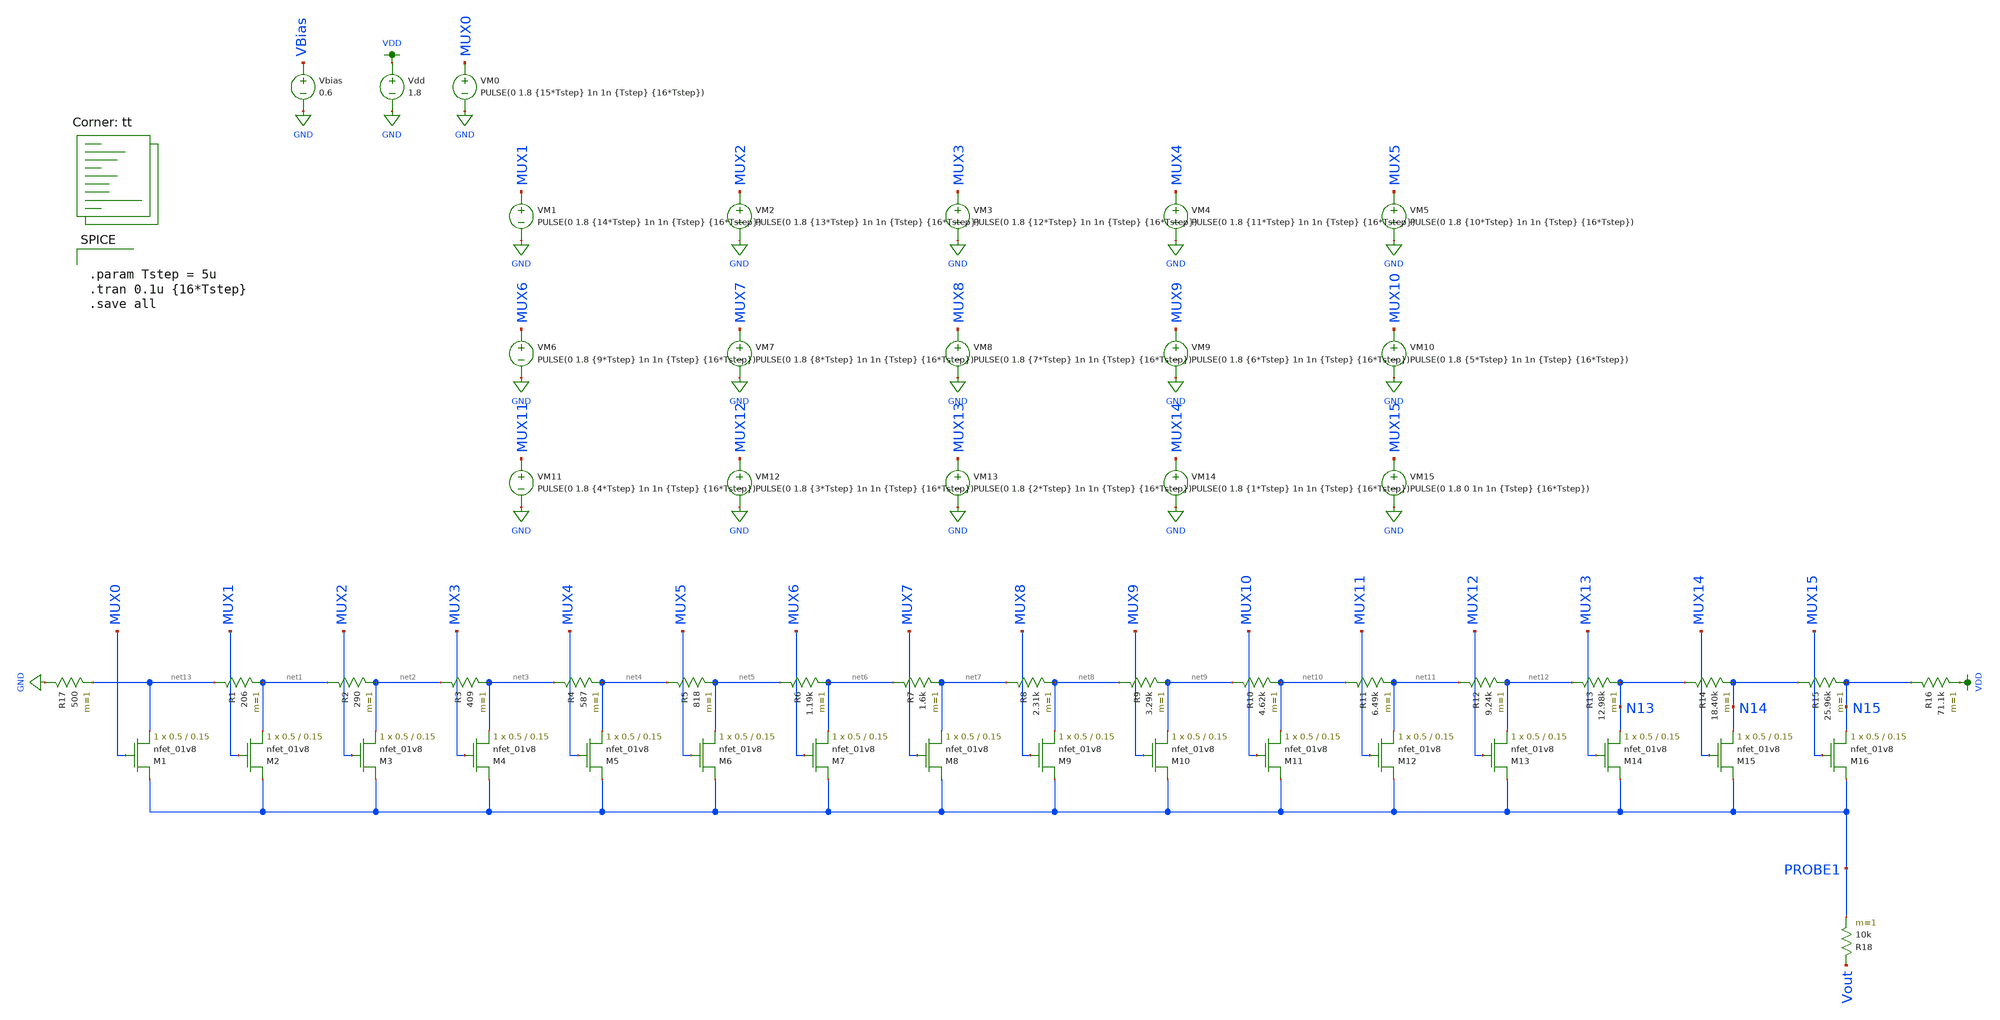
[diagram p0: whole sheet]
** sch_path: DAC/DAC2TB.sch
**.subckt DAC2TB
Vdd VDD GND 1.8
R1 net13 net1 206 m=1
R2 net1 net2 290 m=1
R3 net2 net3 409 m=1
R4 net3 net4 587 m=1
R5 net4 net5 818 m=1
R6 net5 net6 1.19k m=1
R7 net6 net7 1.6k m=1
R8 net7 net8 2.31k m=1
R9 net8 net9 3.29k m=1
R10 net9 net10 4.62k m=1
R11 net10 net11 6.49k m=1
R12 net11 net12 9.24k m=1
R13 net12 N13 12.98k m=1
R14 N13 N14 18.40k m=1
R15 N14 N15 25.96k m=1
R16 N15 VDD 71.1k m=1
XM1 PROBE1 MUX0 net13 GND sky130_fd_pr__nfet_01v8 L=0.15 W=0.5 nf=1 ad='int((nf+1)/2) * W/nf * 0.29'
+ as='int((nf+2)/2) * W/nf * 0.29' pd='2*int((nf+1)/2) * (W/nf + 0.29)' ps='2*int((nf+2)/2) * (W/nf + 0.29)'
+ nrd='0.29 / W' nrs='0.29 / W' sa=0 sb=0 sd=0 mult=1 m=1
VM1 MUX1 GND PULSE(0 1.8 {14*Tstep} 1n 1n {Tstep} {16*Tstep})
VM2 MUX2 GND PULSE(0 1.8 {13*Tstep} 1n 1n {Tstep} {16*Tstep})
VM3 MUX3 GND PULSE(0 1.8 {12*Tstep} 1n 1n {Tstep} {16*Tstep})
VM4 MUX4 GND PULSE(0 1.8 {11*Tstep} 1n 1n {Tstep} {16*Tstep})
VM5 MUX5 GND PULSE(0 1.8 {10*Tstep} 1n 1n {Tstep} {16*Tstep})
VM6 MUX6 GND PULSE(0 1.8 {9*Tstep} 1n 1n {Tstep} {16*Tstep})
VM7 MUX7 GND PULSE(0 1.8 {8*Tstep} 1n 1n {Tstep} {16*Tstep})
VM8 MUX8 GND PULSE(0 1.8 {7*Tstep} 1n 1n {Tstep} {16*Tstep})
VM9 MUX9 GND PULSE(0 1.8 {6*Tstep} 1n 1n {Tstep} {16*Tstep})
VM10 MUX10 GND PULSE(0 1.8 {5*Tstep} 1n 1n {Tstep} {16*Tstep})
VM11 MUX11 GND PULSE(0 1.8 {4*Tstep} 1n 1n {Tstep} {16*Tstep})
VM12 MUX12 GND PULSE(0 1.8 {3*Tstep} 1n 1n {Tstep} {16*Tstep})
VM13 MUX13 GND PULSE(0 1.8 {2*Tstep} 1n 1n {Tstep} {16*Tstep})
VM14 MUX14 GND PULSE(0 1.8 {1*Tstep} 1n 1n {Tstep} {16*Tstep})
VM15 MUX15 GND PULSE(0 1.8 0 1n 1n {Tstep} {16*Tstep})
VM0 MUX0 GND PULSE(0 1.8 {15*Tstep} 1n 1n {Tstep} {16*Tstep})
Vbias VBias GND 0.6
R17 GND net13 500 m=1
R18 Vout PROBE1 10k m=1
XM2 PROBE1 MUX1 net1 GND sky130_fd_pr__nfet_01v8 L=0.15 W=0.5 nf=1 ad='int((nf+1)/2) * W/nf * 0.29' as='int((nf+2)/2) * W/nf * 0.29'
+ pd='2*int((nf+1)/2) * (W/nf + 0.29)' ps='2*int((nf+2)/2) * (W/nf + 0.29)' nrd='0.29 / W' nrs='0.29 / W'
+ sa=0 sb=0 sd=0 mult=1 m=1
XM3 PROBE1 MUX2 net2 GND sky130_fd_pr__nfet_01v8 L=0.15 W=0.5 nf=1 ad='int((nf+1)/2) * W/nf * 0.29' as='int((nf+2)/2) * W/nf * 0.29'
+ pd='2*int((nf+1)/2) * (W/nf + 0.29)' ps='2*int((nf+2)/2) * (W/nf + 0.29)' nrd='0.29 / W' nrs='0.29 / W'
+ sa=0 sb=0 sd=0 mult=1 m=1
XM4 PROBE1 MUX3 net3 GND sky130_fd_pr__nfet_01v8 L=0.15 W=0.5 nf=1 ad='int((nf+1)/2) * W/nf * 0.29' as='int((nf+2)/2) * W/nf * 0.29'
+ pd='2*int((nf+1)/2) * (W/nf + 0.29)' ps='2*int((nf+2)/2) * (W/nf + 0.29)' nrd='0.29 / W' nrs='0.29 / W'
+ sa=0 sb=0 sd=0 mult=1 m=1
XM5 PROBE1 MUX4 net4 GND sky130_fd_pr__nfet_01v8 L=0.15 W=0.5 nf=1 ad='int((nf+1)/2) * W/nf * 0.29' as='int((nf+2)/2) * W/nf * 0.29'
+ pd='2*int((nf+1)/2) * (W/nf + 0.29)' ps='2*int((nf+2)/2) * (W/nf + 0.29)' nrd='0.29 / W' nrs='0.29 / W'
+ sa=0 sb=0 sd=0 mult=1 m=1
XM6 PROBE1 MUX5 net5 GND sky130_fd_pr__nfet_01v8 L=0.15 W=0.5 nf=1 ad='int((nf+1)/2) * W/nf * 0.29' as='int((nf+2)/2) * W/nf * 0.29'
+ pd='2*int((nf+1)/2) * (W/nf + 0.29)' ps='2*int((nf+2)/2) * (W/nf + 0.29)' nrd='0.29 / W' nrs='0.29 / W'
+ sa=0 sb=0 sd=0 mult=1 m=1
XM7 PROBE1 MUX6 net6 GND sky130_fd_pr__nfet_01v8 L=0.15 W=0.5 nf=1 ad='int((nf+1)/2) * W/nf * 0.29' as='int((nf+2)/2) * W/nf * 0.29'
+ pd='2*int((nf+1)/2) * (W/nf + 0.29)' ps='2*int((nf+2)/2) * (W/nf + 0.29)' nrd='0.29 / W' nrs='0.29 / W'
+ sa=0 sb=0 sd=0 mult=1 m=1
XM8 PROBE1 MUX7 net7 GND sky130_fd_pr__nfet_01v8 L=0.15 W=0.5 nf=1 ad='int((nf+1)/2) * W/nf * 0.29' as='int((nf+2)/2) * W/nf * 0.29'
+ pd='2*int((nf+1)/2) * (W/nf + 0.29)' ps='2*int((nf+2)/2) * (W/nf + 0.29)' nrd='0.29 / W' nrs='0.29 / W'
+ sa=0 sb=0 sd=0 mult=1 m=1
XM9 PROBE1 MUX8 net8 GND sky130_fd_pr__nfet_01v8 L=0.15 W=0.5 nf=1 ad='int((nf+1)/2) * W/nf * 0.29' as='int((nf+2)/2) * W/nf * 0.29'
+ pd='2*int((nf+1)/2) * (W/nf + 0.29)' ps='2*int((nf+2)/2) * (W/nf + 0.29)' nrd='0.29 / W' nrs='0.29 / W'
+ sa=0 sb=0 sd=0 mult=1 m=1
XM10 PROBE1 MUX9 net9 GND sky130_fd_pr__nfet_01v8 L=0.15 W=0.5 nf=1 ad='int((nf+1)/2) * W/nf * 0.29'
+ as='int((nf+2)/2) * W/nf * 0.29' pd='2*int((nf+1)/2) * (W/nf + 0.29)' ps='2*int((nf+2)/2) * (W/nf + 0.29)'
+ nrd='0.29 / W' nrs='0.29 / W' sa=0 sb=0 sd=0 mult=1 m=1
XM11 PROBE1 MUX10 net10 GND sky130_fd_pr__nfet_01v8 L=0.15 W=0.5 nf=1 ad='int((nf+1)/2) * W/nf * 0.29'
+ as='int((nf+2)/2) * W/nf * 0.29' pd='2*int((nf+1)/2) * (W/nf + 0.29)' ps='2*int((nf+2)/2) * (W/nf + 0.29)'
+ nrd='0.29 / W' nrs='0.29 / W' sa=0 sb=0 sd=0 mult=1 m=1
XM12 PROBE1 MUX11 net11 GND sky130_fd_pr__nfet_01v8 L=0.15 W=0.5 nf=1 ad='int((nf+1)/2) * W/nf * 0.29'
+ as='int((nf+2)/2) * W/nf * 0.29' pd='2*int((nf+1)/2) * (W/nf + 0.29)' ps='2*int((nf+2)/2) * (W/nf + 0.29)'
+ nrd='0.29 / W' nrs='0.29 / W' sa=0 sb=0 sd=0 mult=1 m=1
XM13 PROBE1 MUX12 net12 GND sky130_fd_pr__nfet_01v8 L=0.15 W=0.5 nf=1 ad='int((nf+1)/2) * W/nf * 0.29'
+ as='int((nf+2)/2) * W/nf * 0.29' pd='2*int((nf+1)/2) * (W/nf + 0.29)' ps='2*int((nf+2)/2) * (W/nf + 0.29)'
+ nrd='0.29 / W' nrs='0.29 / W' sa=0 sb=0 sd=0 mult=1 m=1
XM14 PROBE1 MUX13 N13 GND sky130_fd_pr__nfet_01v8 L=0.15 W=0.5 nf=1 ad='int((nf+1)/2) * W/nf * 0.29'
+ as='int((nf+2)/2) * W/nf * 0.29' pd='2*int((nf+1)/2) * (W/nf + 0.29)' ps='2*int((nf+2)/2) * (W/nf + 0.29)'
+ nrd='0.29 / W' nrs='0.29 / W' sa=0 sb=0 sd=0 mult=1 m=1
XM15 PROBE1 MUX14 N14 GND sky130_fd_pr__nfet_01v8 L=0.15 W=0.5 nf=1 ad='int((nf+1)/2) * W/nf * 0.29'
+ as='int((nf+2)/2) * W/nf * 0.29' pd='2*int((nf+1)/2) * (W/nf + 0.29)' ps='2*int((nf+2)/2) * (W/nf + 0.29)'
+ nrd='0.29 / W' nrs='0.29 / W' sa=0 sb=0 sd=0 mult=1 m=1
XM16 PROBE1 MUX15 N15 GND sky130_fd_pr__nfet_01v8 L=0.15 W=0.5 nf=1 ad='int((nf+1)/2) * W/nf * 0.29'
+ as='int((nf+2)/2) * W/nf * 0.29' pd='2*int((nf+1)/2) * (W/nf + 0.29)' ps='2*int((nf+2)/2) * (W/nf + 0.29)'
+ nrd='0.29 / W' nrs='0.29 / W' sa=0 sb=0 sd=0 mult=1 m=1
**** begin user architecture code


.param Tstep = 5u
.tran 0.1u {16*Tstep}
.save all

.lib $::SKYWATER_MODELS/sky130.lib.spice tt
**** end user architecture code
**.ends
.GLOBAL GND
.GLOBAL VDD
.end
